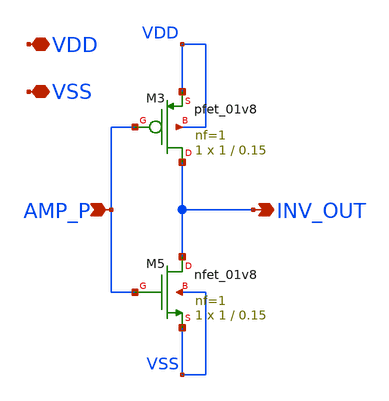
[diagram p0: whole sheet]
** sch_path: xschem/untitled-2.sch
**.subckt untitled-2 AMP_P INV_OUT VDD VSS
*.ipin AMP_P
*.opin INV_OUT
*.iopin VDD
*.iopin VSS
XM3 INV_OUT AMP_P VDD VDD sky130_fd_pr__pfet_01v8 L=0.15 W=1 nf=1 ad='int((nf+1)/2) * W/nf * 0.29' as='int((nf+2)/2) * W/nf * 0.29'
+ pd='2*int((nf+1)/2) * (W/nf + 0.29)' ps='2*int((nf+2)/2) * (W/nf + 0.29)' nrd='0.29 / W' nrs='0.29 / W'
+ sa=0 sb=0 sd=0 mult=1 m=1
XM5 INV_OUT AMP_P VSS VSS sky130_fd_pr__nfet_01v8 L=0.15 W=1 nf=1 ad='int((nf+1)/2) * W/nf * 0.29' as='int((nf+2)/2) * W/nf * 0.29'
+ pd='2*int((nf+1)/2) * (W/nf + 0.29)' ps='2*int((nf+2)/2) * (W/nf + 0.29)' nrd='0.29 / W' nrs='0.29 / W'
+ sa=0 sb=0 sd=0 mult=1 m=1
**.ends
.end
